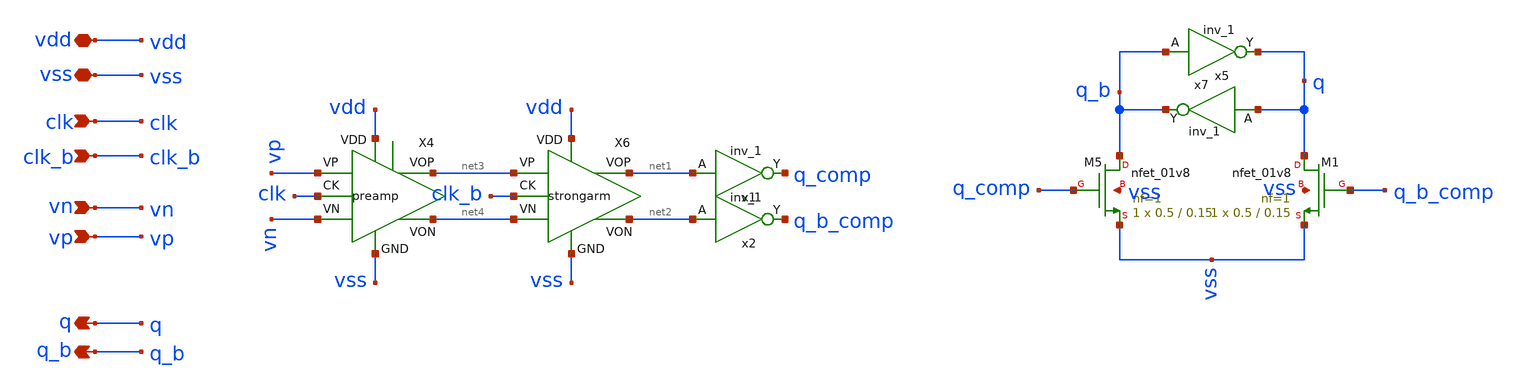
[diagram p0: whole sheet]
** sch_path: xschem/comparator/comparator.sch
**.subckt comparator vp vn vdd clk vss q q_b clk_b
*.ipin vp
*.ipin vn
*.iopin vdd
*.ipin clk
*.iopin vss
*.opin q
*.opin q_b
*.ipin clk_b
X4 vp vn vss net4 net3 vdd clk preamp
X6 net3 net4 vss net2 net1 vdd clk_b strongarm
XM5 q_b q_comp vss vss sky130_fd_pr__nfet_01v8 L=0.15 W=0.5 nf=1 ad='int((1 + 1)/2) * 0.5 / 1 * 0.29'
+ as='int((1 + 2)/2) * 0.5 / 1 * 0.29' pd='2*int((1 + 1)/2) * (0.5 / 1 + 0.29)' ps='2*int((1 + 2)/2) * (0.5 / 1 + 0.29)'
+ nrd='0.29 / 0.5 ' nrs='0.29 / 0.5 ' sa=0 sb=0 sd=0 mult=1 m=1
XM1 q q_b_comp vss vss sky130_fd_pr__nfet_01v8 L=0.15 W=0.5 nf=1 ad='int((1 + 1)/2) * 0.5 / 1 * 0.29'
+ as='int((1 + 2)/2) * 0.5 / 1 * 0.29' pd='2*int((1 + 1)/2) * (0.5 / 1 + 0.29)' ps='2*int((1 + 2)/2) * (0.5 / 1 + 0.29)'
+ nrd='0.29 / 0.5 ' nrs='0.29 / 0.5 ' sa=0 sb=0 sd=0 mult=1 m=1
x5 q_b vss vss vdd vdd q sky130_fd_sc_hd__inv_1
x7 q vss vss vdd vdd q_b sky130_fd_sc_hd__inv_1
x1 net1 vss vss vdd vdd q_comp sky130_fd_sc_hd__inv_1
x2 net2 vss vss vdd vdd q_b_comp sky130_fd_sc_hd__inv_1
**.ends

* expanding   symbol:  xschem/comparator/preamp.sym # of pins=7
** sym_path: xschem/comparator/preamp.sym
** sch_path: xschem/comparator/preamp.sch
.subckt preamp VP VN GND VON VOP VDD CK
*.iopin VDD
*.iopin GND
*.iopin CK
*.iopin VON
*.iopin VOP
*.iopin VP
*.iopin VN
XM5 VON VP net1 GND sky130_fd_pr__nfet_01v8 L=1.5 W=2 nf=2 ad='int((2 + 1)/2) * 2 / 2 * 0.29' as='int((2 + 2)/2) * 2 / 2 * 0.29'
+ pd='2*int((2 + 1)/2) * (2 / 2 + 0.29)' ps='2*int((2 + 2)/2) * (2 / 2 + 0.29)' nrd='0.29 / 2 ' nrs='0.29 / 2 '
+ sa=0 sb=0 sd=0 mult=1 m=1
XM6 VON VON VDD VDD sky130_fd_pr__pfet_01v8 L=1.5 W=4 nf=1 ad='int((nf+1)/2) * W/nf * 0.29' as='int((nf+2)/2) * W/nf * 0.29'
+ pd='2*int((nf+1)/2) * (W/nf + 0.29)' ps='2*int((nf+2)/2) * (W/nf + 0.29)' nrd='0.29 / W' nrs='0.29 / W'
+ sa=0 sb=0 sd=0 mult=1 m=1
XM7 VOP VOP VDD VDD sky130_fd_pr__pfet_01v8 L=1.5 W=4 nf=1 ad='int((nf+1)/2) * W/nf * 0.29' as='int((nf+2)/2) * W/nf * 0.29'
+ pd='2*int((nf+1)/2) * (W/nf + 0.29)' ps='2*int((nf+2)/2) * (W/nf + 0.29)' nrd='0.29 / W' nrs='0.29 / W'
+ sa=0 sb=0 sd=0 mult=1 m=1
XM8 VOP VN net1 GND sky130_fd_pr__nfet_01v8 L=1.5 W=2 nf=2 ad='int((2 + 1)/2) * 2 / 2 * 0.29' as='int((2 + 2)/2) * 2 / 2 * 0.29'
+ pd='2*int((2 + 1)/2) * (2 / 2 + 0.29)' ps='2*int((2 + 2)/2) * (2 / 2 + 0.29)' nrd='0.29 / 2 ' nrs='0.29 / 2 '
+ sa=0 sb=0 sd=0 mult=1 m=1
XM9 net1 CK GND GND sky130_fd_pr__nfet_01v8 L=1 W=4 nf=1 ad='int((1 + 1)/2) * 4 / 1 * 0.29' as='int((1 + 2)/2) * 4 / 1 * 0.29'
+ pd='2*int((1 + 1)/2) * (4 / 1 + 0.29)' ps='2*int((1 + 2)/2) * (4 / 1 + 0.29)' nrd='0.29 / 4 ' nrs='0.29 / 4 '
+ sa=0 sb=0 sd=0 mult=1 m=1
.ends


* expanding   symbol:  xschem/comparator/strongarm.sym # of pins=7
** sym_path: xschem/comparator/strongarm.sym
** sch_path: xschem/comparator/strongarm.sch
.subckt strongarm VP VN GND VON VOP VDD CK
*.iopin GND
*.ipin VP
*.opin VOP
*.opin VON
*.ipin VN
*.iopin VDD
*.ipin CK
XM2 net2 CK GND GND sky130_fd_pr__nfet_01v8 L=0.15 W=2 nf=2 ad='int((nf+1)/2) * W/nf * 0.29' as='int((nf+2)/2) * W/nf * 0.29'
+ pd='2*int((nf+1)/2) * (W/nf + 0.29)' ps='2*int((nf+2)/2) * (W/nf + 0.29)' nrd='0.29 / W' nrs='0.29 / W'
+ sa=0 sb=0 sd=0 mult=1 m=1
XM4 VON CK VDD VDD sky130_fd_pr__pfet_01v8 L=0.15 W=1 nf=1 ad='int((nf+1)/2) * W/nf * 0.29' as='int((nf+2)/2) * W/nf * 0.29'
+ pd='2*int((nf+1)/2) * (W/nf + 0.29)' ps='2*int((nf+2)/2) * (W/nf + 0.29)' nrd='0.29 / W' nrs='0.29 / W'
+ sa=0 sb=0 sd=0 mult=1 m=1
XM5 net1 CK VDD VDD sky130_fd_pr__pfet_01v8 L=0.15 W=1 nf=1 ad='int((nf+1)/2) * W/nf * 0.29' as='int((nf+2)/2) * W/nf * 0.29'
+ pd='2*int((nf+1)/2) * (W/nf + 0.29)' ps='2*int((nf+2)/2) * (W/nf + 0.29)' nrd='0.29 / W' nrs='0.29 / W'
+ sa=0 sb=0 sd=0 mult=1 m=1
XM8 net1 VP net2 GND sky130_fd_pr__nfet_01v8 L=0.15 W=2.5 nf=4 ad='int((nf+1)/2) * W/nf * 0.29' as='int((nf+2)/2) * W/nf * 0.29'
+ pd='2*int((nf+1)/2) * (W/nf + 0.29)' ps='2*int((nf+2)/2) * (W/nf + 0.29)' nrd='0.29 / W' nrs='0.29 / W'
+ sa=0 sb=0 sd=0 mult=1 m=1
XM9 VON VOP net1 GND sky130_fd_pr__nfet_01v8 L=0.15 W=2.5 nf=4 ad='int((nf+1)/2) * W/nf * 0.29' as='int((nf+2)/2) * W/nf * 0.29'
+ pd='2*int((nf+1)/2) * (W/nf + 0.29)' ps='2*int((nf+2)/2) * (W/nf + 0.29)' nrd='0.29 / W' nrs='0.29 / W'
+ sa=0 sb=0 sd=0 mult=1 m=1
XM10 VON VOP VDD VDD sky130_fd_pr__pfet_01v8 L=0.15 W=2.5 nf=1 ad='int((nf+1)/2) * W/nf * 0.29' as='int((nf+2)/2) * W/nf * 0.29'
+ pd='2*int((nf+1)/2) * (W/nf + 0.29)' ps='2*int((nf+2)/2) * (W/nf + 0.29)' nrd='0.29 / W' nrs='0.29 / W'
+ sa=0 sb=0 sd=0 mult=1 m=1
XM11 VOP CK VDD VDD sky130_fd_pr__pfet_01v8 L=0.15 W=1 nf=1 ad='int((nf+1)/2) * W/nf * 0.29' as='int((nf+2)/2) * W/nf * 0.29'
+ pd='2*int((nf+1)/2) * (W/nf + 0.29)' ps='2*int((nf+2)/2) * (W/nf + 0.29)' nrd='0.29 / W' nrs='0.29 / W'
+ sa=0 sb=0 sd=0 mult=1 m=1
XM12 net3 CK VDD VDD sky130_fd_pr__pfet_01v8 L=0.15 W=1 nf=1 ad='int((nf+1)/2) * W/nf * 0.29' as='int((nf+2)/2) * W/nf * 0.29'
+ pd='2*int((nf+1)/2) * (W/nf + 0.29)' ps='2*int((nf+2)/2) * (W/nf + 0.29)' nrd='0.29 / W' nrs='0.29 / W'
+ sa=0 sb=0 sd=0 mult=1 m=1
XM13 net3 VN net2 GND sky130_fd_pr__nfet_01v8 L=0.15 W=2.5 nf=4 ad='int((nf+1)/2) * W/nf * 0.29' as='int((nf+2)/2) * W/nf * 0.29'
+ pd='2*int((nf+1)/2) * (W/nf + 0.29)' ps='2*int((nf+2)/2) * (W/nf + 0.29)' nrd='0.29 / W' nrs='0.29 / W'
+ sa=0 sb=0 sd=0 mult=1 m=1
XM14 VOP VON net3 GND sky130_fd_pr__nfet_01v8 L=0.15 W=10 nf=1 ad='int((nf+1)/2) * W/nf * 0.29' as='int((nf+2)/2) * W/nf * 0.29'
+ pd='2*int((nf+1)/2) * (W/nf + 0.29)' ps='2*int((nf+2)/2) * (W/nf + 0.29)' nrd='0.29 / W' nrs='0.29 / W'
+ sa=0 sb=0 sd=0 mult=1 m=1
XM15 VOP VON VDD VDD sky130_fd_pr__pfet_01v8 L=0.15 W=2.5 nf=1 ad='int((nf+1)/2) * W/nf * 0.29' as='int((nf+2)/2) * W/nf * 0.29'
+ pd='2*int((nf+1)/2) * (W/nf + 0.29)' ps='2*int((nf+2)/2) * (W/nf + 0.29)' nrd='0.29 / W' nrs='0.29 / W'
+ sa=0 sb=0 sd=0 mult=1 m=1
.ends

.end
